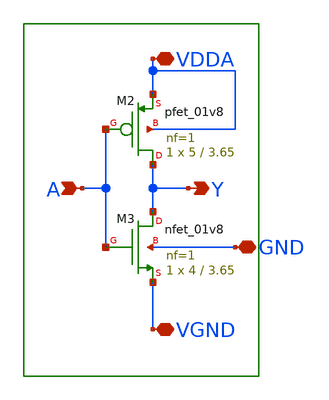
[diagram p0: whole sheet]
** sch_path: xschem/lib/aux_inv.sch
**.subckt aux_inv VDDA VGND A Y GND
*.iopin VDDA
*.iopin VGND
*.ipin A
*.opin Y
*.iopin GND
XM3 Y A VGND GND sky130_fd_pr__nfet_01v8 L=3.65 W=4 nf=1 ad='int((nf+1)/2) * W/nf * 0.29' as='int((nf+2)/2) * W/nf * 0.29'
+ pd='2*int((nf+1)/2) * (W/nf + 0.29)' ps='2*int((nf+2)/2) * (W/nf + 0.29)' nrd='0.29 / W' nrs='0.29 / W'
+ sa=0 sb=0 sd=0 mult=1 m=1
XM2 Y A VDDA VDDA sky130_fd_pr__pfet_01v8 L=3.65 W=5 nf=1 ad='int((nf+1)/2) * W/nf * 0.29' as='int((nf+2)/2) * W/nf * 0.29'
+ pd='2*int((nf+1)/2) * (W/nf + 0.29)' ps='2*int((nf+2)/2) * (W/nf + 0.29)' nrd='0.29 / W' nrs='0.29 / W'
+ sa=0 sb=0 sd=0 mult=1 m=1
**.ends
.end
